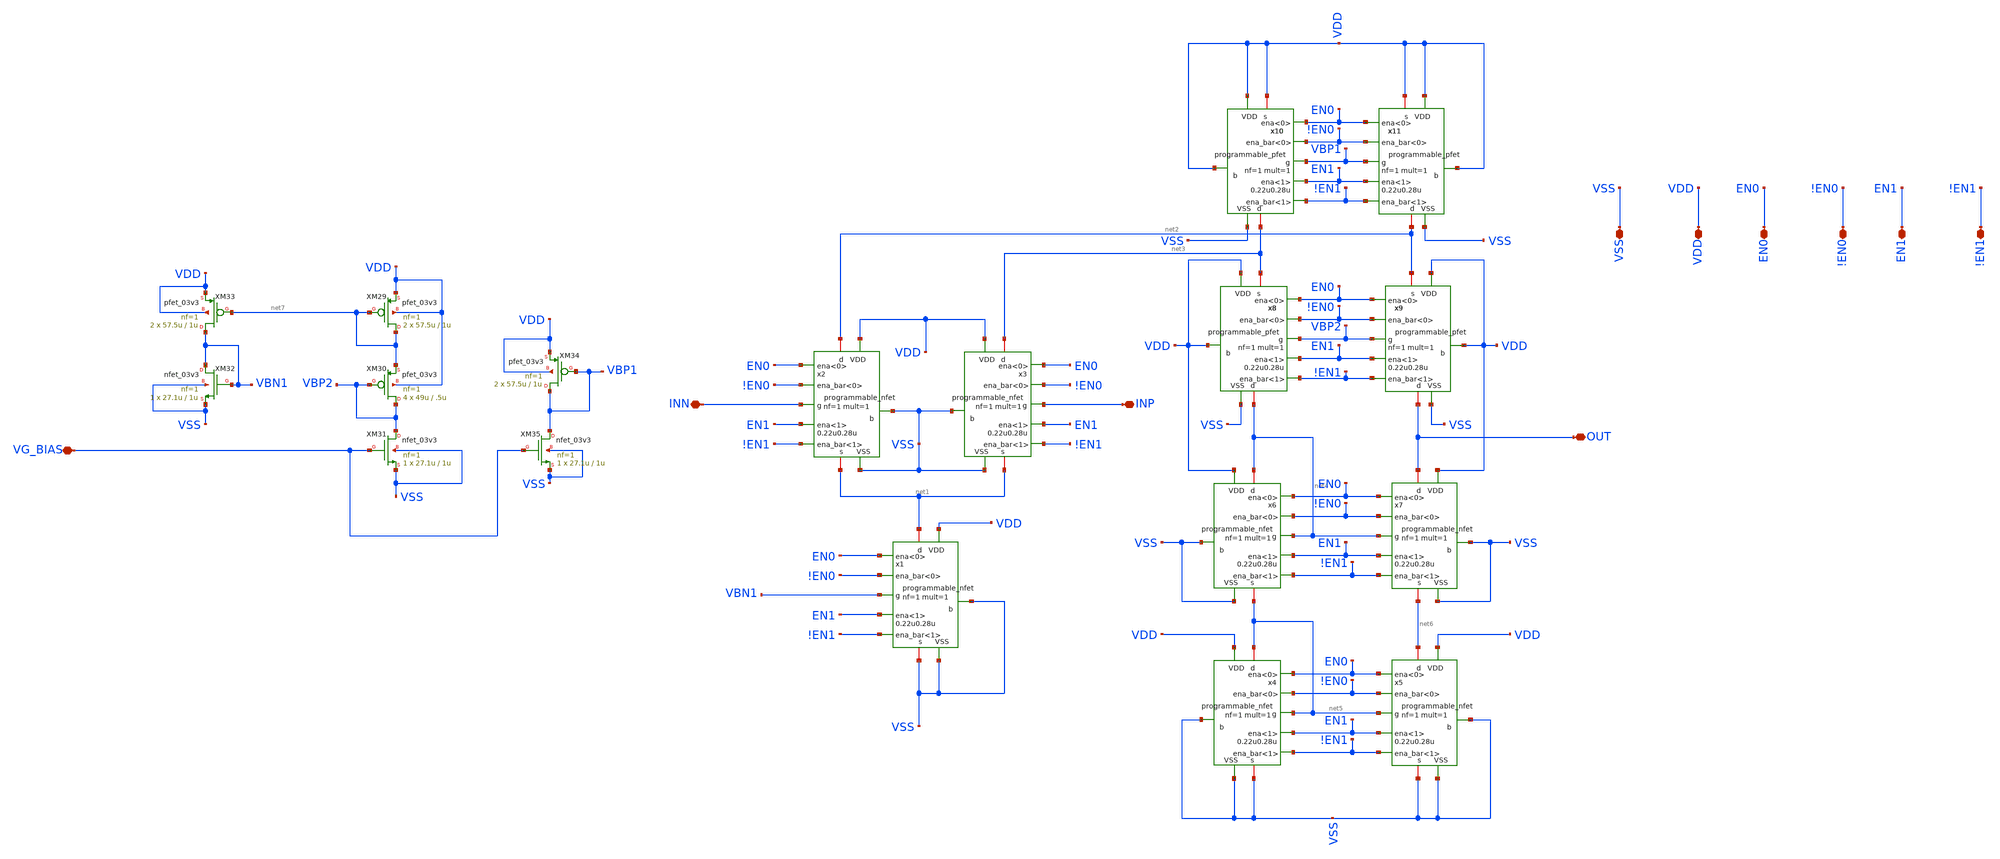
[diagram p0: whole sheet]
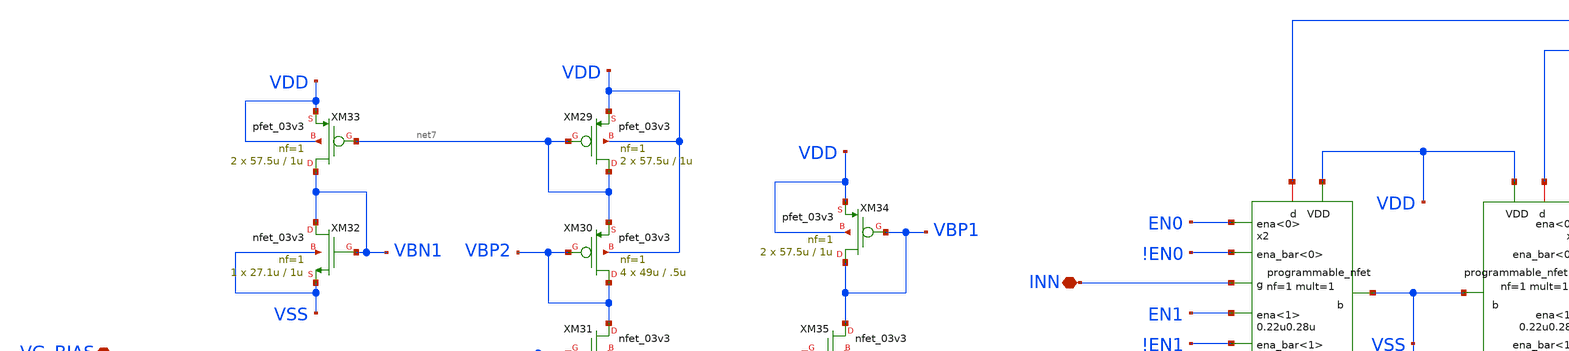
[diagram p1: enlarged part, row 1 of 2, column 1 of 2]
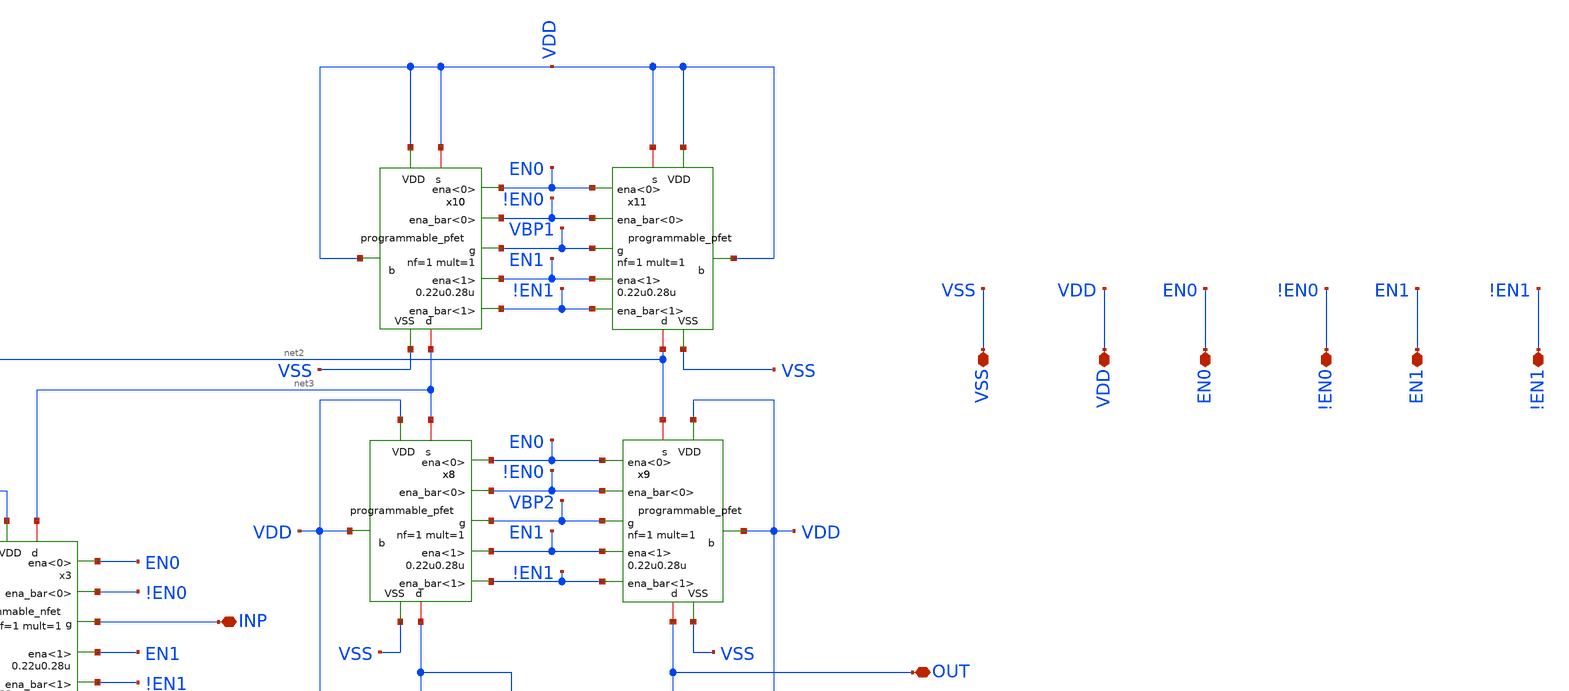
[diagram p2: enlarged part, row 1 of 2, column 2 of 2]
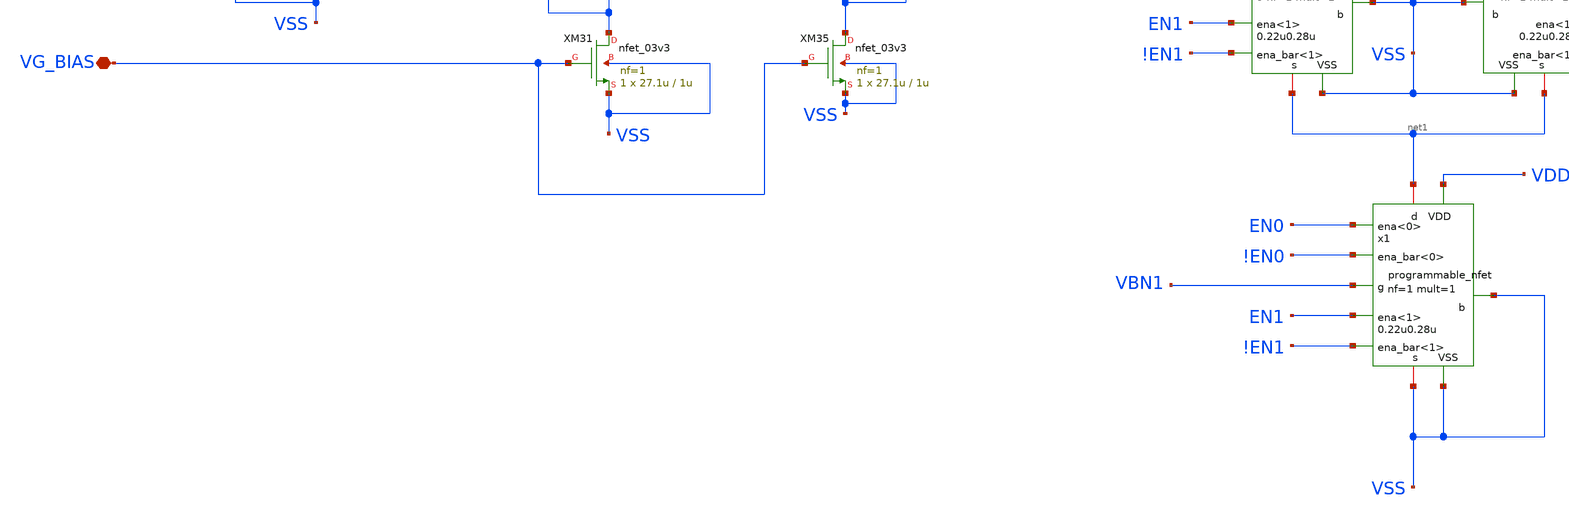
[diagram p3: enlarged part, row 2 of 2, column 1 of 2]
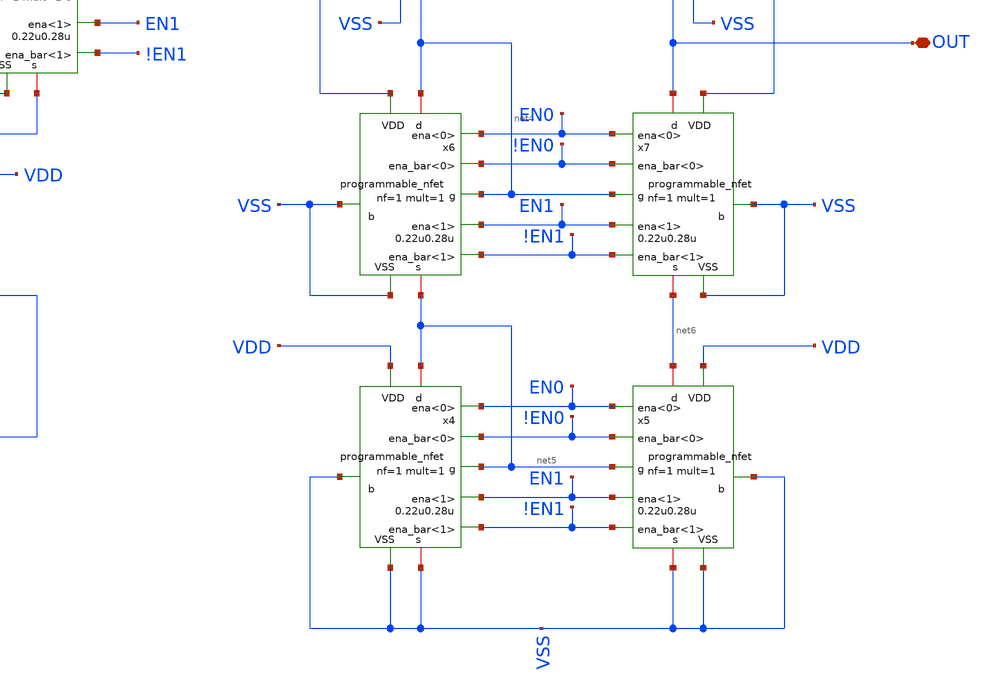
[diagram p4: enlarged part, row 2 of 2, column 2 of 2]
** sch_path: designs/libs/old_files/old_amps/ota_folded_cascode/programmable_folded.sch
**.subckt programmable_folded OUT VSS VDD EN0 !EN0 EN1 !EN1 INN INP VG_BIAS
*.iopin OUT
*.iopin VSS
*.iopin VDD
*.iopin EN0
*.iopin !EN0
*.iopin EN1
*.iopin !EN1
*.iopin INN
*.iopin INP
*.iopin VG_BIAS
XM29 net7 net7 VDD VDD pfet_03v3 L=1u W=57.5u nf=1 ad='int((nf+1)/2) * W/nf * 0.18u' as='int((nf+2)/2) * W/nf * 0.18u'
+ pd='2*int((nf+1)/2) * (W/nf + 0.18u)' ps='2*int((nf+2)/2) * (W/nf + 0.18u)' nrd='0.18u / W' nrs='0.18u / W'
+ sa=0 sb=0 sd=0 m=2
XM30 VBP2 VBP2 net7 VDD pfet_03v3 L=.5u W=49u nf=1 ad='int((nf+1)/2) * W/nf * 0.18u' as='int((nf+2)/2) * W/nf * 0.18u'
+ pd='2*int((nf+1)/2) * (W/nf + 0.18u)' ps='2*int((nf+2)/2) * (W/nf + 0.18u)' nrd='0.18u / W' nrs='0.18u / W'
+ sa=0 sb=0 sd=0 m=4
XM31 VBP2 VG_BIAS VSS VSS nfet_03v3 L=1u W=27.1u nf=1 ad='int((nf+1)/2) * W/nf * 0.18u' as='int((nf+2)/2) * W/nf * 0.18u'
+ pd='2*int((nf+1)/2) * (W/nf + 0.18u)' ps='2*int((nf+2)/2) * (W/nf + 0.18u)' nrd='0.18u / W' nrs='0.18u / W'
+ sa=0 sb=0 sd=0 m=1
XM32 VBN1 VBN1 VSS VSS nfet_03v3 L=1u W=27.1u nf=1 ad='int((nf+1)/2) * W/nf * 0.18u' as='int((nf+2)/2) * W/nf * 0.18u'
+ pd='2*int((nf+1)/2) * (W/nf + 0.18u)' ps='2*int((nf+2)/2) * (W/nf + 0.18u)' nrd='0.18u / W' nrs='0.18u / W'
+ sa=0 sb=0 sd=0 m=1
XM33 VBN1 net7 VDD VDD pfet_03v3 L=1u W=57.5u nf=1 ad='int((nf+1)/2) * W/nf * 0.18u' as='int((nf+2)/2) * W/nf * 0.18u'
+ pd='2*int((nf+1)/2) * (W/nf + 0.18u)' ps='2*int((nf+2)/2) * (W/nf + 0.18u)' nrd='0.18u / W' nrs='0.18u / W'
+ sa=0 sb=0 sd=0 m=2
XM34 VBP1 VBP1 VDD VDD pfet_03v3 L=1u W=57.5u nf=1 ad='int((nf+1)/2) * W/nf * 0.18u' as='int((nf+2)/2) * W/nf * 0.18u'
+ pd='2*int((nf+1)/2) * (W/nf + 0.18u)' ps='2*int((nf+2)/2) * (W/nf + 0.18u)' nrd='0.18u / W' nrs='0.18u / W'
+ sa=0 sb=0 sd=0 m=2
XM35 VBP1 VG_BIAS VSS VSS nfet_03v3 L=1u W=27.1u nf=1 ad='int((nf+1)/2) * W/nf * 0.18u' as='int((nf+2)/2) * W/nf * 0.18u'
+ pd='2*int((nf+1)/2) * (W/nf + 0.18u)' ps='2*int((nf+2)/2) * (W/nf + 0.18u)' nrd='0.18u / W' nrs='0.18u / W'
+ sa=0 sb=0 sd=0 m=1
x1 net1 VSS VBN1 VSS !EN0 VDD !EN1 EN0 EN1 VSS programmable_nfet width=0.22u length=0.28u nf=1
+ mult=1
x2 net2 VSS INN net1 !EN0 VDD !EN1 EN0 EN1 VSS programmable_nfet width=0.22u length=0.28u nf=1
+ mult=1
x3 net3 VSS INP net1 !EN0 VDD !EN1 EN0 EN1 VSS programmable_nfet width=0.22u length=0.28u nf=1
+ mult=1
x4 net5 VSS net5 VSS !EN0 VDD !EN1 EN0 EN1 VSS programmable_nfet width=0.22u length=0.28u nf=1
+ mult=1
x5 net6 VSS net5 VSS !EN0 VDD !EN1 EN0 EN1 VSS programmable_nfet width=0.22u length=0.28u nf=1
+ mult=1
x6 net4 VSS net4 net5 !EN0 VDD !EN1 EN0 EN1 VSS programmable_nfet width=0.22u length=0.28u nf=1
+ mult=1
x7 OUT VSS net4 net6 !EN0 VDD !EN1 EN0 EN1 VSS programmable_nfet width=0.22u length=0.28u nf=1
+ mult=1
x8 net4 VDD VBP2 net3 !EN0 VDD !EN1 EN0 EN1 VSS programmable_pfet width=0.22u length=0.28u nf=1
+ mult=1
x9 OUT VDD VBP2 net2 !EN0 VDD !EN1 EN0 EN1 VSS programmable_pfet width=0.22u length=0.28u nf=1
+ mult=1
x10 net3 VDD VBP1 VDD !EN0 VDD !EN1 EN0 EN1 VSS programmable_pfet width=0.22u length=0.28u nf=1
+ mult=1
x11 net2 VDD VBP1 VDD !EN0 VDD !EN1 EN0 EN1 VSS programmable_pfet width=0.22u length=0.28u nf=1
+ mult=1
**.ends

* expanding   symbol:  libs/core_digital/schem/programmable_nfet.sym # of pins=10
** sym_path: designs/libs/core_digital/schem/programmable_nfet.sym
** sch_path: designs/libs/core_digital/schem/programmable_nfet.sch
.subckt programmable_nfet d b g s ena_bar<0> VDD ena_bar<1> ena<0> ena<1> VSS  width=0.22u
+ length=0.28u nf=1 mult=1
*.ipin VSS
*.ipin VDD
*.ipin g
*.ipin ena_bar<1>
*.ipin ena_bar<0>
*.ipin ena<1>
*.ipin ena<0>
*.iopin d
*.iopin s
*.ipin b
XM1 d net2 s b nfet_03v3 L={length} W={width} nf={nf} ad='int((nf+1)/2) * W/nf * 0.18u' as='int((nf+2)/2) * W/nf * 0.18u'
+ pd='2*int((nf+1)/2) * (W/nf + 0.18u)' ps='2*int((nf+2)/2) * (W/nf + 0.18u)' nrd='0.18u / W' nrs='0.18u / W'
+ sa=0 sb=0 sd=0 m={mult}
XM3 d net1 s b nfet_03v3 L={length} W={2*width} nf={2*nf} ad='int((nf+1)/2) * W/nf * 0.18u' as='int((nf+2)/2) * W/nf * 0.18u'
+ pd='2*int((nf+1)/2) * (W/nf + 0.18u)' ps='2*int((nf+2)/2) * (W/nf + 0.18u)' nrd='0.18u / W' nrs='0.18u / W'
+ sa=0 sb=0 sd=0 m={mult}
XM2 net1 ena_bar<1> VSS VSS nfet_03v3 L=0.28u W=0.22u nf=1 ad='int((nf+1)/2) * W/nf * 0.18u' as='int((nf+2)/2) * W/nf * 0.18u'
+ pd='2*int((nf+1)/2) * (W/nf + 0.18u)' ps='2*int((nf+2)/2) * (W/nf + 0.18u)' nrd='0.18u / W' nrs='0.18u / W'
+ sa=0 sb=0 sd=0 m=1
XM4 net2 ena_bar<0> VSS VSS nfet_03v3 L=0.28u W=0.22u nf=1 ad='int((nf+1)/2) * W/nf * 0.18u' as='int((nf+2)/2) * W/nf * 0.18u'
+ pd='2*int((nf+1)/2) * (W/nf + 0.18u)' ps='2*int((nf+2)/2) * (W/nf + 0.18u)' nrd='0.18u / W' nrs='0.18u / W'
+ sa=0 sb=0 sd=0 m=1
x1 ena_bar<0> VDD net2 g VSS ena<0> transmission_gate
x2 ena_bar<1> VDD net1 g VSS ena<1> transmission_gate
.ends


* expanding   symbol:  libs/core_digital/schem/programmable_pfet.sym # of pins=10
** sym_path: designs/libs/core_digital/schem/programmable_pfet.sym
** sch_path: designs/libs/core_digital/schem/programmable_pfet.sch
.subckt programmable_pfet d b g s ena_bar<0> VDD ena_bar<1> ena<0> ena<1> VSS  width=0.22u
+ length=0.28u nf=1 mult=1
*.ipin VSS
*.ipin VDD
*.ipin g
*.ipin ena_bar<1>
*.ipin ena_bar<0>
*.ipin ena<0>
*.iopin s
*.iopin d
*.ipin b
*.ipin ena<1>
XM1 d net2 s b pfet_03v3 L={length} W={width} nf={nf} ad='int((nf+1)/2) * W/nf * 0.18u' as='int((nf+2)/2) * W/nf * 0.18u'
+ pd='2*int((nf+1)/2) * (W/nf + 0.18u)' ps='2*int((nf+2)/2) * (W/nf + 0.18u)' nrd='0.18u / W' nrs='0.18u / W'
+ sa=0 sb=0 sd=0 m={mult}
XM3 d net1 s b pfet_03v3 L={length} W={2*width} nf={2*nf} ad='int((nf+1)/2) * W/nf * 0.18u' as='int((nf+2)/2) * W/nf * 0.18u'
+ pd='2*int((nf+1)/2) * (W/nf + 0.18u)' ps='2*int((nf+2)/2) * (W/nf + 0.18u)' nrd='0.18u / W' nrs='0.18u / W'
+ sa=0 sb=0 sd=0 m={mult}
XM2 net1 ena<1> VDD VDD pfet_03v3 L=0.28u W=0.22u nf=1 ad='int((nf+1)/2) * W/nf * 0.18u' as='int((nf+2)/2) * W/nf * 0.18u'
+ pd='2*int((nf+1)/2) * (W/nf + 0.18u)' ps='2*int((nf+2)/2) * (W/nf + 0.18u)' nrd='0.18u / W' nrs='0.18u / W'
+ sa=0 sb=0 sd=0 m=1
XM4 net2 ena<0> VDD VDD pfet_03v3 L=0.28u W=0.22u nf=1 ad='int((nf+1)/2) * W/nf * 0.18u' as='int((nf+2)/2) * W/nf * 0.18u'
+ pd='2*int((nf+1)/2) * (W/nf + 0.18u)' ps='2*int((nf+2)/2) * (W/nf + 0.18u)' nrd='0.18u / W' nrs='0.18u / W'
+ sa=0 sb=0 sd=0 m=1
x1 ena_bar<0> VDD net2 g VSS ena<0> transmission_gate
x2 ena_bar<1> VDD net1 g VSS ena<1> transmission_gate
.ends


* expanding   symbol:  libs/core_digital/schem/transmission_gate.sym # of pins=6
** sym_path: designs/libs/core_digital/schem/transmission_gate.sym
** sch_path: designs/libs/core_digital/schem/transmission_gate.sch
.subckt transmission_gate ena_bar VDD out in VSS ena
*.ipin in
*.ipin ena_bar
*.ipin ena
*.ipin VSS
*.ipin VDD
*.opin out
XM1 in ena_bar out VDD pfet_03v3 L=0.28u W=0.22u nf=1 ad='int((nf+1)/2) * W/nf * 0.18u' as='int((nf+2)/2) * W/nf * 0.18u'
+ pd='2*int((nf+1)/2) * (W/nf + 0.18u)' ps='2*int((nf+2)/2) * (W/nf + 0.18u)' nrd='0.18u / W' nrs='0.18u / W'
+ sa=0 sb=0 sd=0 m=1
XM2 in ena out VSS nfet_03v3 L=0.28u W=0.22u nf=1 ad='int((nf+1)/2) * W/nf * 0.18u' as='int((nf+2)/2) * W/nf * 0.18u'
+ pd='2*int((nf+1)/2) * (W/nf + 0.18u)' ps='2*int((nf+2)/2) * (W/nf + 0.18u)' nrd='0.18u / W' nrs='0.18u / W'
+ sa=0 sb=0 sd=0 m=1
.ends

.end
